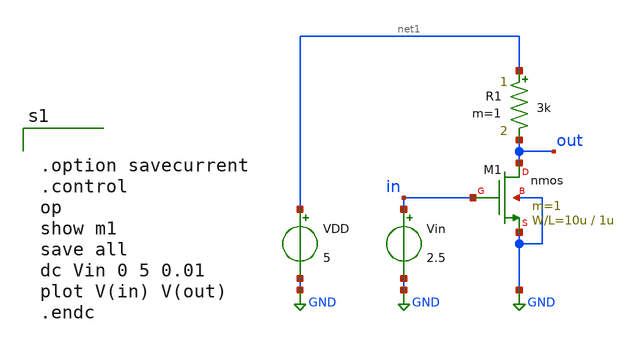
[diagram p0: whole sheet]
** sch_path: member_project/GroupWork/Team_masahiro/nfet_common_source_DC.sch
**.subckt nfet_common_source_DC
M1 out in GND GND nmos L=1u W=10u m=1
R1 net1 out 3k m=1
VDD net1 GND 5
Vin in GND 2.5
**** begin user architecture code
 .include $::LIB/mos.lib
.include $::LIB/passive.lib
.include $::LIB/diode.lib


.option savecurrent
.control
op
show m1
save all
dc Vin 0 5 0.01
plot V(in) V(out)
.endc


**** end user architecture code
**.ends
.GLOBAL GND
.end
